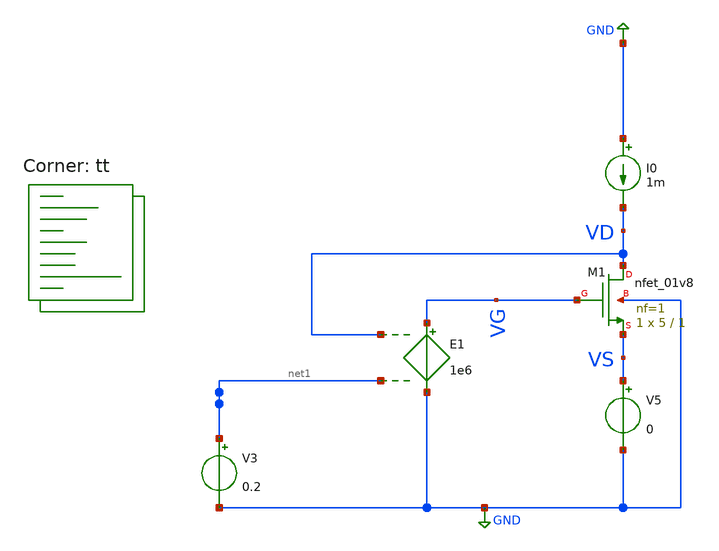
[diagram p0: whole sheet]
** sch_path: userLib/SizingTB.sch
**.subckt SizingTB
XM1 VD VG VS GND sky130_fd_pr__nfet_01v8 L=1 W=5 nf=1 ad='int((nf+1)/2) * W/nf * 0.29' as='int((nf+2)/2) * W/nf * 0.29'
+ pd='2*int((nf+1)/2) * (W/nf + 0.29)' ps='2*int((nf+2)/2) * (W/nf + 0.29)' nrd='0.29 / W' nrs='0.29 / W'
+ sa=0 sb=0 sd=0 mult=1 m=1
E1 VG GND VD net1 1e6
V5 VS GND 0
V3 net1 GND 0.2
I0 GND VD 1m
**** begin user architecture code

* this option enables mos model bin
* selection based on W/NF instead of W
.option wnflag=1
.option savecurrents


.control
save all





save @m.xm1.msky130_fd_pr__nfet_01v8[id]
save @m.xm1.msky130_fd_pr__nfet_01v8[gm]
save @m.xm1.msky130_fd_pr__nfet_01v8[gds]
save @m.xm1.msky130_fd_pr__nfet_01v8[vgs]
save @m.xm1.msky130_fd_pr__nfet_01v8[vds]
save @m.xm1.msky130_fd_pr__nfet_01v8[vth]
save @m.xm1.msky130_fd_pr__nfet_01v8[vdsat]






  dc I0 1u 400u 1u


  plot all.@m.xm1.msky130_fd_pr__nfet_01v8[id]
  plot all.@m.xm1.msky130_fd_pr__nfet_01v8[gm]
  plot all.@m.xm1.msky130_fd_pr__nfet_01v8[gds]
  plot all.@m.xm1.msky130_fd_pr__nfet_01v8[vds]
  plot all.@m.xm1.msky130_fd_pr__nfet_01v8[vgs]
  plot all.@m.xm1.msky130_fd_pr__nfet_01v8[vth]


  set appendwrite
 set filetype=binary
 write SizingTB.raw

.endc



.lib $::SKYWATER_MODELS/sky130.lib.spice tt
**** end user architecture code
**.ends
.GLOBAL GND
.end
